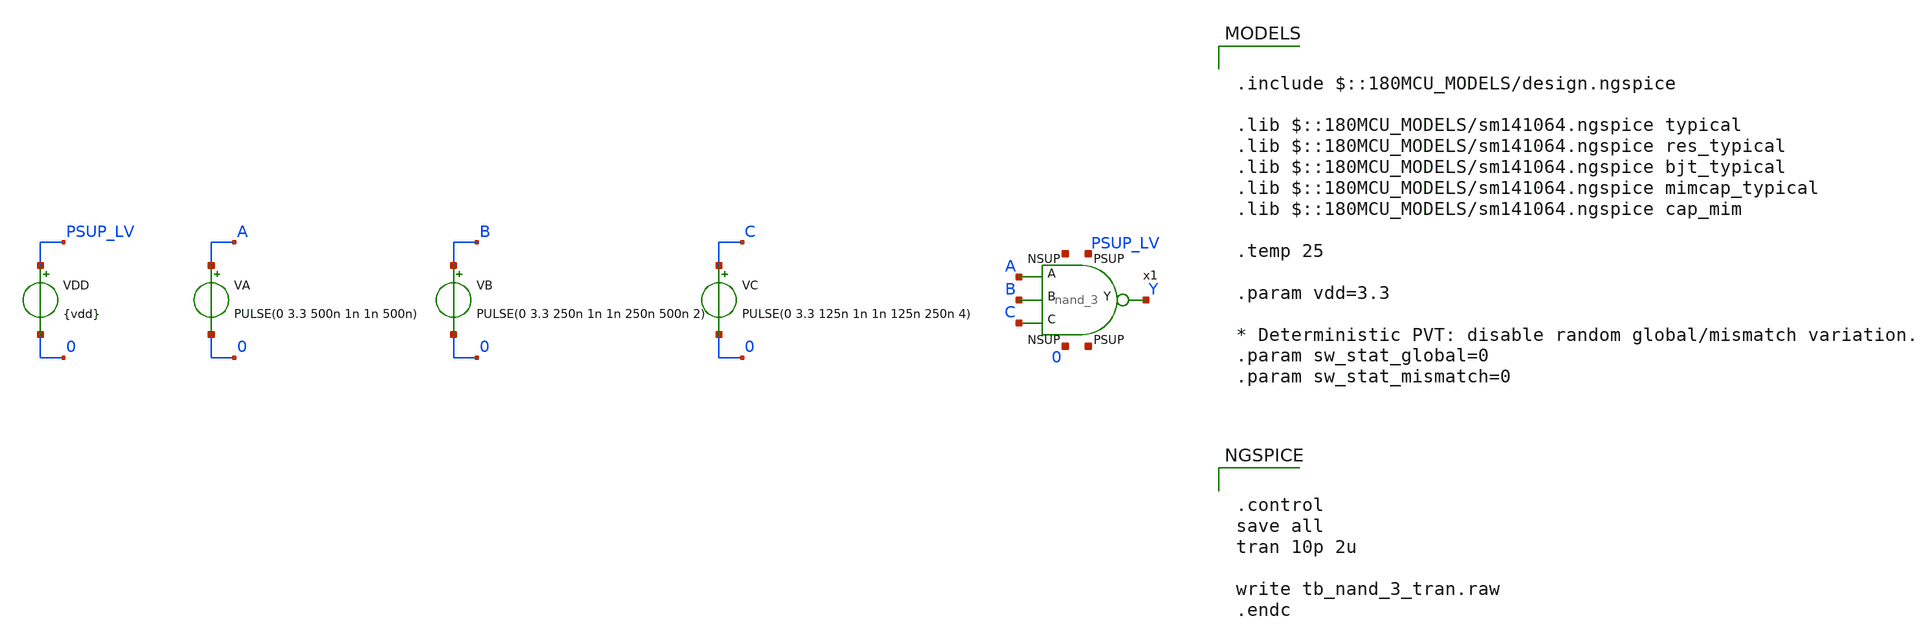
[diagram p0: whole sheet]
** sch_path: xschem/blocks/nand_3/tb_nand_3_tran.sch
**.subckt tb_nand_3_tran
VB B 0 PULSE(0 3.3 250n 1n 1n 250n 500n 2)
VA A 0 PULSE(0 3.3 500n 1n 1n 500n)
VDD PSUP_LV 0 {vdd}
x1 Y A C PSUP_LV 0 B nand_3
VC C 0 PULSE(0 3.3 125n 1n 1n 125n 250n 4)
**** begin user architecture code

.include $::180MCU_MODELS/design.ngspice

.lib $::180MCU_MODELS/sm141064.ngspice typical
.lib $::180MCU_MODELS/sm141064.ngspice res_typical
.lib $::180MCU_MODELS/sm141064.ngspice bjt_typical
.lib $::180MCU_MODELS/sm141064.ngspice mimcap_typical
.lib $::180MCU_MODELS/sm141064.ngspice cap_mim

.temp 25

.param vdd=3.3

* Deterministic PVT: disable random global/mismatch variation.
.param sw_stat_global=0
.param sw_stat_mismatch=0



.control
save all
tran 10p 2u

write tb_nand_3_tran.raw
.endc


**** end user architecture code
**.ends

* expanding   symbol:  blocks/nand_3/nand_3.sym # of pins=8
** sym_path: xschem/blocks/nand_3/nand_3.sym
** sch_path: xschem/blocks/nand_3/nand_3.sch
.subckt nand_3 Y A C PSUP NSUP B
*.ipin PSUP
*.ipin NSUP
*.ipin A
*.ipin B
*.opin Y
*.ipin C
XM5 net1 C NSUP NSUP nfet_03v3 L=0.28u W=0.22u nf=1 ad='int((nf+1)/2) * W/nf * 0.18u' as='int((nf+2)/2) * W/nf * 0.18u'
+ pd='2*int((nf+1)/2) * (W/nf + 0.18u)' ps='2*int((nf+2)/2) * (W/nf + 0.18u)' nrd='0.18u / W' nrs='0.18u / W'
+ sa=0 sb=0 sd=0 m=1
XM1 Y A net2 NSUP nfet_03v3 L=0.28u W=0.22u nf=1 ad='int((nf+1)/2) * W/nf * 0.18u' as='int((nf+2)/2) * W/nf * 0.18u'
+ pd='2*int((nf+1)/2) * (W/nf + 0.18u)' ps='2*int((nf+2)/2) * (W/nf + 0.18u)' nrd='0.18u / W' nrs='0.18u / W'
+ sa=0 sb=0 sd=0 m=1
XM2 Y C PSUP PSUP pfet_03v3 L=0.28u W=0.5u nf=1 ad='int((nf+1)/2) * W/nf * 0.18u' as='int((nf+2)/2) * W/nf * 0.18u'
+ pd='2*int((nf+1)/2) * (W/nf + 0.18u)' ps='2*int((nf+2)/2) * (W/nf + 0.18u)' nrd='0.18u / W' nrs='0.18u / W'
+ sa=0 sb=0 sd=0 m=1
XM3 Y B PSUP PSUP pfet_03v3 L=0.28u W=0.5u nf=1 ad='int((nf+1)/2) * W/nf * 0.18u' as='int((nf+2)/2) * W/nf * 0.18u'
+ pd='2*int((nf+1)/2) * (W/nf + 0.18u)' ps='2*int((nf+2)/2) * (W/nf + 0.18u)' nrd='0.18u / W' nrs='0.18u / W'
+ sa=0 sb=0 sd=0 m=1
XM4 net2 B net1 NSUP nfet_03v3 L=0.28u W=0.22u nf=1 ad='int((nf+1)/2) * W/nf * 0.18u' as='int((nf+2)/2) * W/nf * 0.18u'
+ pd='2*int((nf+1)/2) * (W/nf + 0.18u)' ps='2*int((nf+2)/2) * (W/nf + 0.18u)' nrd='0.18u / W' nrs='0.18u / W'
+ sa=0 sb=0 sd=0 m=1
XM6 Y A PSUP PSUP pfet_03v3 L=0.28u W=0.5u nf=1 ad='int((nf+1)/2) * W/nf * 0.18u' as='int((nf+2)/2) * W/nf * 0.18u'
+ pd='2*int((nf+1)/2) * (W/nf + 0.18u)' ps='2*int((nf+2)/2) * (W/nf + 0.18u)' nrd='0.18u / W' nrs='0.18u / W'
+ sa=0 sb=0 sd=0 m=1
.ends

.end
